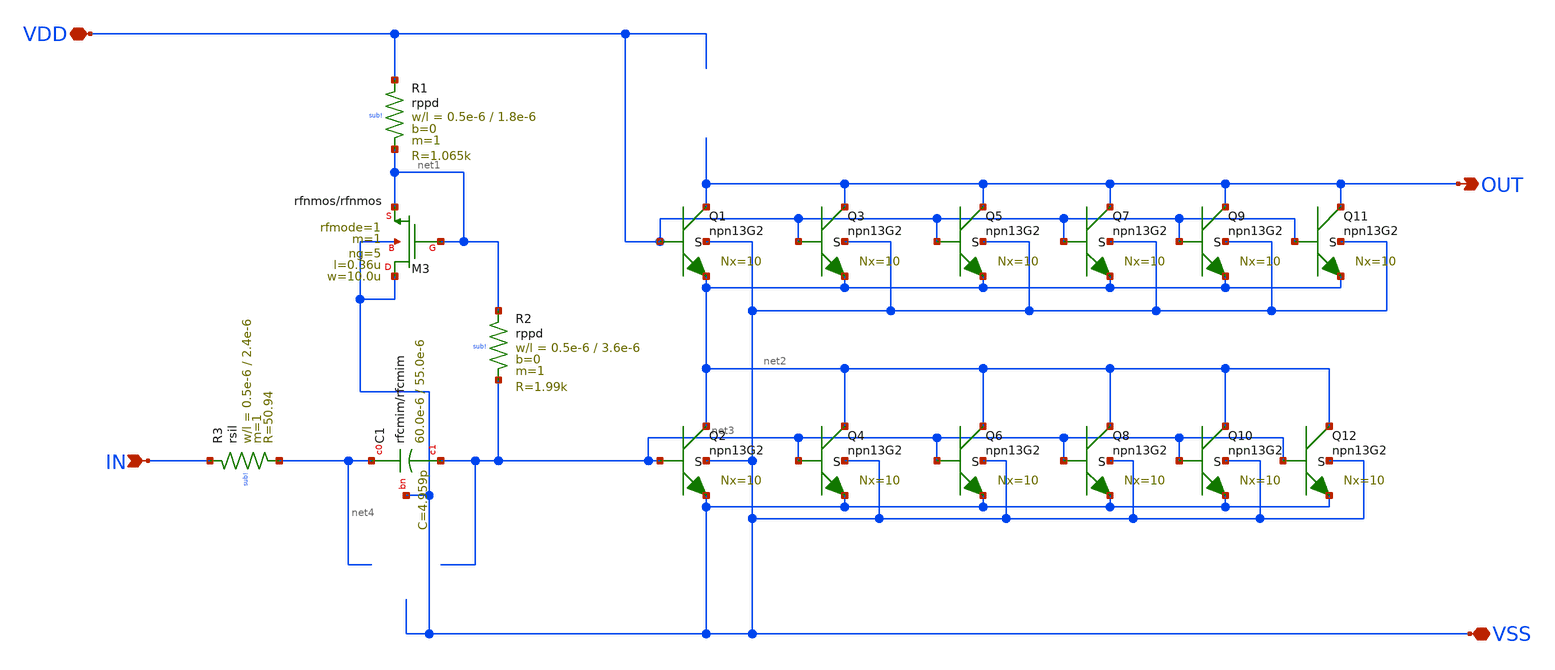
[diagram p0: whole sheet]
** sch_path: GPS_LNA/design_data/lvs/lna_full_base_lvs.sch
**.subckt lna_full_base_lvs VDD IN OUT VSS
*.iopin VDD
*.ipin IN
*.opin OUT
*.iopin VSS
XR2 net1 net3 sub! rppd w=0.5e-6 l=3.6e-6 m=1 b=0 mm_ok=1
XR1 VDD net1 sub! rppd w=0.5e-6 l=1.8e-6 m=1 b=0 mm_ok=1
XR3 IN net4 sub! rsil w=0.5e-6 l=2.4e-6 m=1 mm_ok=1
XC1 net4 net3 VSS rfcmim w=60.0e-6 l=55.0e-6 wfeed=5.0e-6 m=1 mm_ok=1
XM3 VSS net1 net1 VSS rfnmos w=10.0u l=0.36u ng=5 m=1 rfmode=1 mm_ok=1
XQ1 OUT VDD net2 VSS npn13G2 Nx=10 mm_ok=1
XQ2 net2 net3 VSS VSS npn13G2 Nx=10 mm_ok=1
XQ3 OUT VDD net2 VSS npn13G2 Nx=10 mm_ok=1
XQ4 net2 net3 VSS VSS npn13G2 Nx=10 mm_ok=1
XQ5 OUT VDD net2 VSS npn13G2 Nx=10 mm_ok=1
XQ6 net2 net3 VSS VSS npn13G2 Nx=10 mm_ok=1
XQ7 OUT VDD net2 VSS npn13G2 Nx=10 mm_ok=1
XQ8 net2 net3 VSS VSS npn13G2 Nx=10 mm_ok=1
XQ9 OUT VDD net2 VSS npn13G2 Nx=10 mm_ok=1
XQ10 net2 net3 VSS VSS npn13G2 Nx=10 mm_ok=1
XQ11 OUT VDD net2 VSS npn13G2 Nx=10 mm_ok=1
XQ12 net2 net3 VSS VSS npn13G2 Nx=10 mm_ok=1
**.ends
.end
